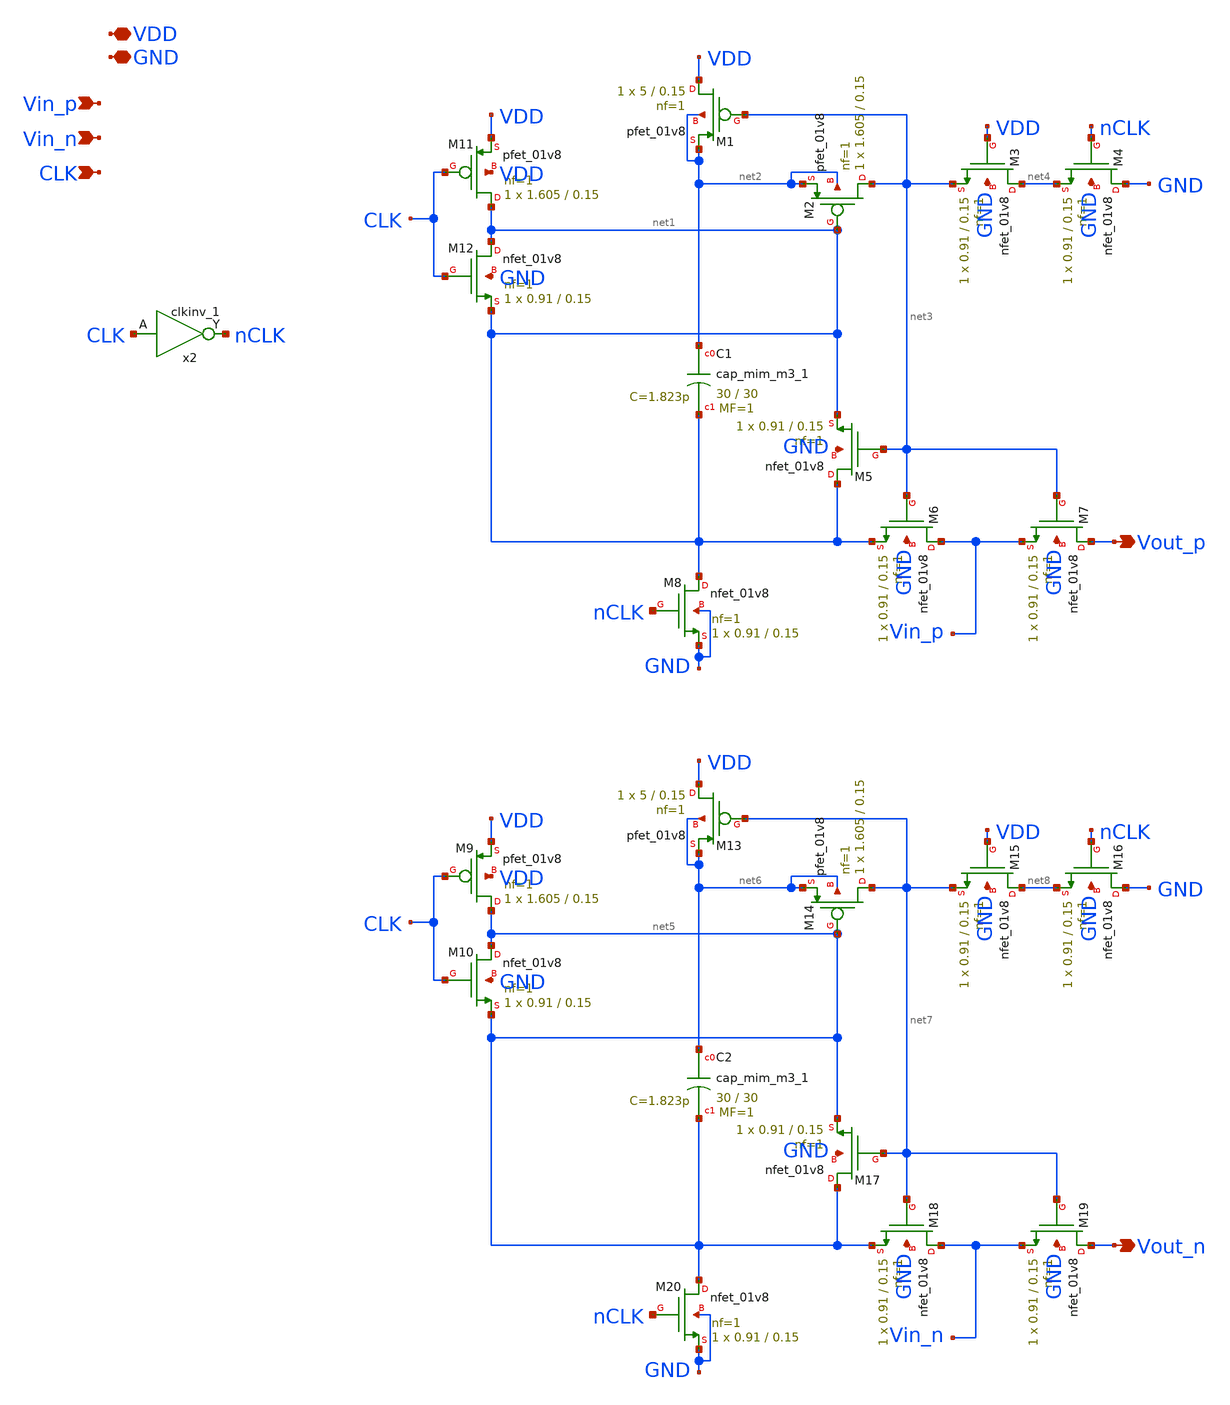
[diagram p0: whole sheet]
** sch_path: xschem/bsswitch.sch
**.subckt bsswitch Vin_p Vin_n CLK Vout_p Vout_n VDD GND
*.ipin Vin_p
*.ipin Vin_n
*.ipin CLK
*.opin Vout_p
*.opin Vout_n
*.iopin VDD
*.iopin GND
XM11 net1 CLK VDD VDD sky130_fd_pr__pfet_01v8 L=0.15 W=1.605 nf=1 ad='int((nf+1)/2) * W/nf * 0.29' as='int((nf+2)/2) * W/nf * 0.29'
+ pd='2*int((nf+1)/2) * (W/nf + 0.29)' ps='2*int((nf+2)/2) * (W/nf + 0.29)' nrd='0.29 / W' nrs='0.29 / W'
+ sa=0 sb=0 sd=0 mult=1 m=1
XM12 net1 CLK net1 GND sky130_fd_pr__nfet_01v8 L=0.15 W=0.91 nf=1 ad='int((nf+1)/2) * W/nf * 0.29' as='int((nf+2)/2) * W/nf * 0.29'
+ pd='2*int((nf+1)/2) * (W/nf + 0.29)' ps='2*int((nf+2)/2) * (W/nf + 0.29)' nrd='0.29 / W' nrs='0.29 / W'
+ sa=0 sb=0 sd=0 mult=1 m=1
XM1 VDD net3 net2 net2 sky130_fd_pr__pfet_01v8 L=0.15 W=5 nf=1 ad='int((nf+1)/2) * W/nf * 0.29' as='int((nf+2)/2) * W/nf * 0.29'
+ pd='2*int((nf+1)/2) * (W/nf + 0.29)' ps='2*int((nf+2)/2) * (W/nf + 0.29)' nrd='0.29 / W' nrs='0.29 / W'
+ sa=0 sb=0 sd=0 mult=1 m=1
XC1 net2 net1 sky130_fd_pr__cap_mim_m3_1 W=30 L=30 MF=1 m=1
XM2 net3 net1 net2 net2 sky130_fd_pr__pfet_01v8 L=0.15 W=1.605 nf=1 ad='int((nf+1)/2) * W/nf * 0.29'
+ as='int((nf+2)/2) * W/nf * 0.29' pd='2*int((nf+1)/2) * (W/nf + 0.29)' ps='2*int((nf+2)/2) * (W/nf + 0.29)'
+ nrd='0.29 / W' nrs='0.29 / W' sa=0 sb=0 sd=0 mult=1 m=1
XM3 net4 VDD net3 GND sky130_fd_pr__nfet_01v8 L=0.15 W=0.91 nf=1 ad='int((nf+1)/2) * W/nf * 0.29' as='int((nf+2)/2) * W/nf * 0.29'
+ pd='2*int((nf+1)/2) * (W/nf + 0.29)' ps='2*int((nf+2)/2) * (W/nf + 0.29)' nrd='0.29 / W' nrs='0.29 / W'
+ sa=0 sb=0 sd=0 mult=1 m=1
XM4 GND nCLK net4 GND sky130_fd_pr__nfet_01v8 L=0.15 W=0.91 nf=1 ad='int((nf+1)/2) * W/nf * 0.29' as='int((nf+2)/2) * W/nf * 0.29'
+ pd='2*int((nf+1)/2) * (W/nf + 0.29)' ps='2*int((nf+2)/2) * (W/nf + 0.29)' nrd='0.29 / W' nrs='0.29 / W'
+ sa=0 sb=0 sd=0 mult=1 m=1
XM5 net1 net3 net1 GND sky130_fd_pr__nfet_01v8 L=0.15 W=0.91 nf=1 ad='int((nf+1)/2) * W/nf * 0.29' as='int((nf+2)/2) * W/nf * 0.29'
+ pd='2*int((nf+1)/2) * (W/nf + 0.29)' ps='2*int((nf+2)/2) * (W/nf + 0.29)' nrd='0.29 / W' nrs='0.29 / W'
+ sa=0 sb=0 sd=0 mult=1 m=1
XM6 Vin_p net3 net1 GND sky130_fd_pr__nfet_01v8 L=0.15 W=0.91 nf=1 ad='int((nf+1)/2) * W/nf * 0.29' as='int((nf+2)/2) * W/nf * 0.29'
+ pd='2*int((nf+1)/2) * (W/nf + 0.29)' ps='2*int((nf+2)/2) * (W/nf + 0.29)' nrd='0.29 / W' nrs='0.29 / W'
+ sa=0 sb=0 sd=0 mult=1 m=1
XM7 Vout_p net3 Vin_p GND sky130_fd_pr__nfet_01v8 L=0.15 W=0.91 nf=1 ad='int((nf+1)/2) * W/nf * 0.29'
+ as='int((nf+2)/2) * W/nf * 0.29' pd='2*int((nf+1)/2) * (W/nf + 0.29)' ps='2*int((nf+2)/2) * (W/nf + 0.29)'
+ nrd='0.29 / W' nrs='0.29 / W' sa=0 sb=0 sd=0 mult=1 m=1
XM8 net1 nCLK GND GND sky130_fd_pr__nfet_01v8 L=0.15 W=0.91 nf=1 ad='int((nf+1)/2) * W/nf * 0.29' as='int((nf+2)/2) * W/nf * 0.29'
+ pd='2*int((nf+1)/2) * (W/nf + 0.29)' ps='2*int((nf+2)/2) * (W/nf + 0.29)' nrd='0.29 / W' nrs='0.29 / W'
+ sa=0 sb=0 sd=0 mult=1 m=1
XM9 net5 CLK VDD VDD sky130_fd_pr__pfet_01v8 L=0.15 W=1.605 nf=1 ad='int((nf+1)/2) * W/nf * 0.29' as='int((nf+2)/2) * W/nf * 0.29'
+ pd='2*int((nf+1)/2) * (W/nf + 0.29)' ps='2*int((nf+2)/2) * (W/nf + 0.29)' nrd='0.29 / W' nrs='0.29 / W'
+ sa=0 sb=0 sd=0 mult=1 m=1
XM10 net5 CLK net5 GND sky130_fd_pr__nfet_01v8 L=0.15 W=0.91 nf=1 ad='int((nf+1)/2) * W/nf * 0.29' as='int((nf+2)/2) * W/nf * 0.29'
+ pd='2*int((nf+1)/2) * (W/nf + 0.29)' ps='2*int((nf+2)/2) * (W/nf + 0.29)' nrd='0.29 / W' nrs='0.29 / W'
+ sa=0 sb=0 sd=0 mult=1 m=1
XM13 VDD net7 net6 net6 sky130_fd_pr__pfet_01v8 L=0.15 W=5 nf=1 ad='int((nf+1)/2) * W/nf * 0.29' as='int((nf+2)/2) * W/nf * 0.29'
+ pd='2*int((nf+1)/2) * (W/nf + 0.29)' ps='2*int((nf+2)/2) * (W/nf + 0.29)' nrd='0.29 / W' nrs='0.29 / W'
+ sa=0 sb=0 sd=0 mult=1 m=1
XC2 net6 net5 sky130_fd_pr__cap_mim_m3_1 W=30 L=30 MF=1 m=1
XM14 net7 net5 net6 net6 sky130_fd_pr__pfet_01v8 L=0.15 W=1.605 nf=1 ad='int((nf+1)/2) * W/nf * 0.29'
+ as='int((nf+2)/2) * W/nf * 0.29' pd='2*int((nf+1)/2) * (W/nf + 0.29)' ps='2*int((nf+2)/2) * (W/nf + 0.29)'
+ nrd='0.29 / W' nrs='0.29 / W' sa=0 sb=0 sd=0 mult=1 m=1
XM15 net8 VDD net7 GND sky130_fd_pr__nfet_01v8 L=0.15 W=0.91 nf=1 ad='int((nf+1)/2) * W/nf * 0.29' as='int((nf+2)/2) * W/nf * 0.29'
+ pd='2*int((nf+1)/2) * (W/nf + 0.29)' ps='2*int((nf+2)/2) * (W/nf + 0.29)' nrd='0.29 / W' nrs='0.29 / W'
+ sa=0 sb=0 sd=0 mult=1 m=1
XM16 GND nCLK net8 GND sky130_fd_pr__nfet_01v8 L=0.15 W=0.91 nf=1 ad='int((nf+1)/2) * W/nf * 0.29' as='int((nf+2)/2) * W/nf * 0.29'
+ pd='2*int((nf+1)/2) * (W/nf + 0.29)' ps='2*int((nf+2)/2) * (W/nf + 0.29)' nrd='0.29 / W' nrs='0.29 / W'
+ sa=0 sb=0 sd=0 mult=1 m=1
XM17 net5 net7 net5 GND sky130_fd_pr__nfet_01v8 L=0.15 W=0.91 nf=1 ad='int((nf+1)/2) * W/nf * 0.29' as='int((nf+2)/2) * W/nf * 0.29'
+ pd='2*int((nf+1)/2) * (W/nf + 0.29)' ps='2*int((nf+2)/2) * (W/nf + 0.29)' nrd='0.29 / W' nrs='0.29 / W'
+ sa=0 sb=0 sd=0 mult=1 m=1
XM18 Vin_n net7 net5 GND sky130_fd_pr__nfet_01v8 L=0.15 W=0.91 nf=1 ad='int((nf+1)/2) * W/nf * 0.29'
+ as='int((nf+2)/2) * W/nf * 0.29' pd='2*int((nf+1)/2) * (W/nf + 0.29)' ps='2*int((nf+2)/2) * (W/nf + 0.29)'
+ nrd='0.29 / W' nrs='0.29 / W' sa=0 sb=0 sd=0 mult=1 m=1
XM19 Vout_n net7 Vin_n GND sky130_fd_pr__nfet_01v8 L=0.15 W=0.91 nf=1 ad='int((nf+1)/2) * W/nf * 0.29'
+ as='int((nf+2)/2) * W/nf * 0.29' pd='2*int((nf+1)/2) * (W/nf + 0.29)' ps='2*int((nf+2)/2) * (W/nf + 0.29)'
+ nrd='0.29 / W' nrs='0.29 / W' sa=0 sb=0 sd=0 mult=1 m=1
XM20 net5 nCLK GND GND sky130_fd_pr__nfet_01v8 L=0.15 W=0.91 nf=1 ad='int((nf+1)/2) * W/nf * 0.29' as='int((nf+2)/2) * W/nf * 0.29'
+ pd='2*int((nf+1)/2) * (W/nf + 0.29)' ps='2*int((nf+2)/2) * (W/nf + 0.29)' nrd='0.29 / W' nrs='0.29 / W'
+ sa=0 sb=0 sd=0 mult=1 m=1
x2 CLK VGND VNB VPB VPWR nCLK sky130_fd_sc_hd__clkinv_1
**.ends
.end
